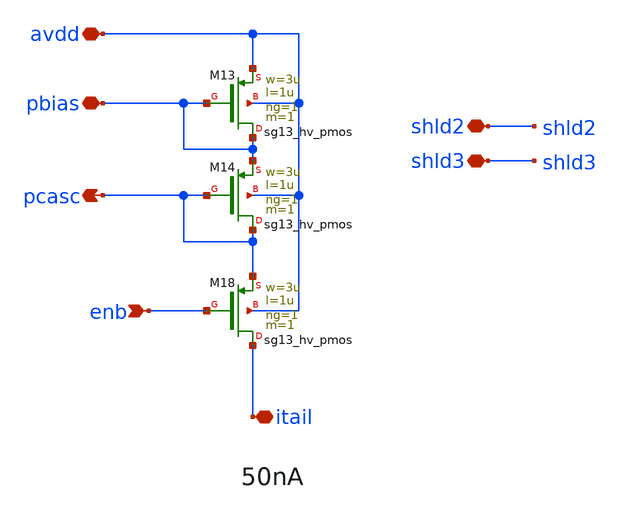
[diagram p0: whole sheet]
** sch_path: xschem/bias_pset2.sch
**.subckt bias_pset2 pbias itail enb pcasc avdd shld2 shld3
*.iopin pbias
*.iopin itail
*.ipin enb
*.opin pcasc
*.iopin avdd
*.iopin shld2
*.iopin shld3
XM13 pbias pbias avdd avdd sg13_hv_pmos w=3u l=1u ng=1 m=1 mm_ok=1
XM18 itail enb pcasc avdd sg13_hv_pmos w=3u l=1u ng=1 m=1 mm_ok=1
XM14 pcasc pcasc pbias avdd sg13_hv_pmos w=3u l=1u ng=1 m=1 mm_ok=1
**.ends
.end
